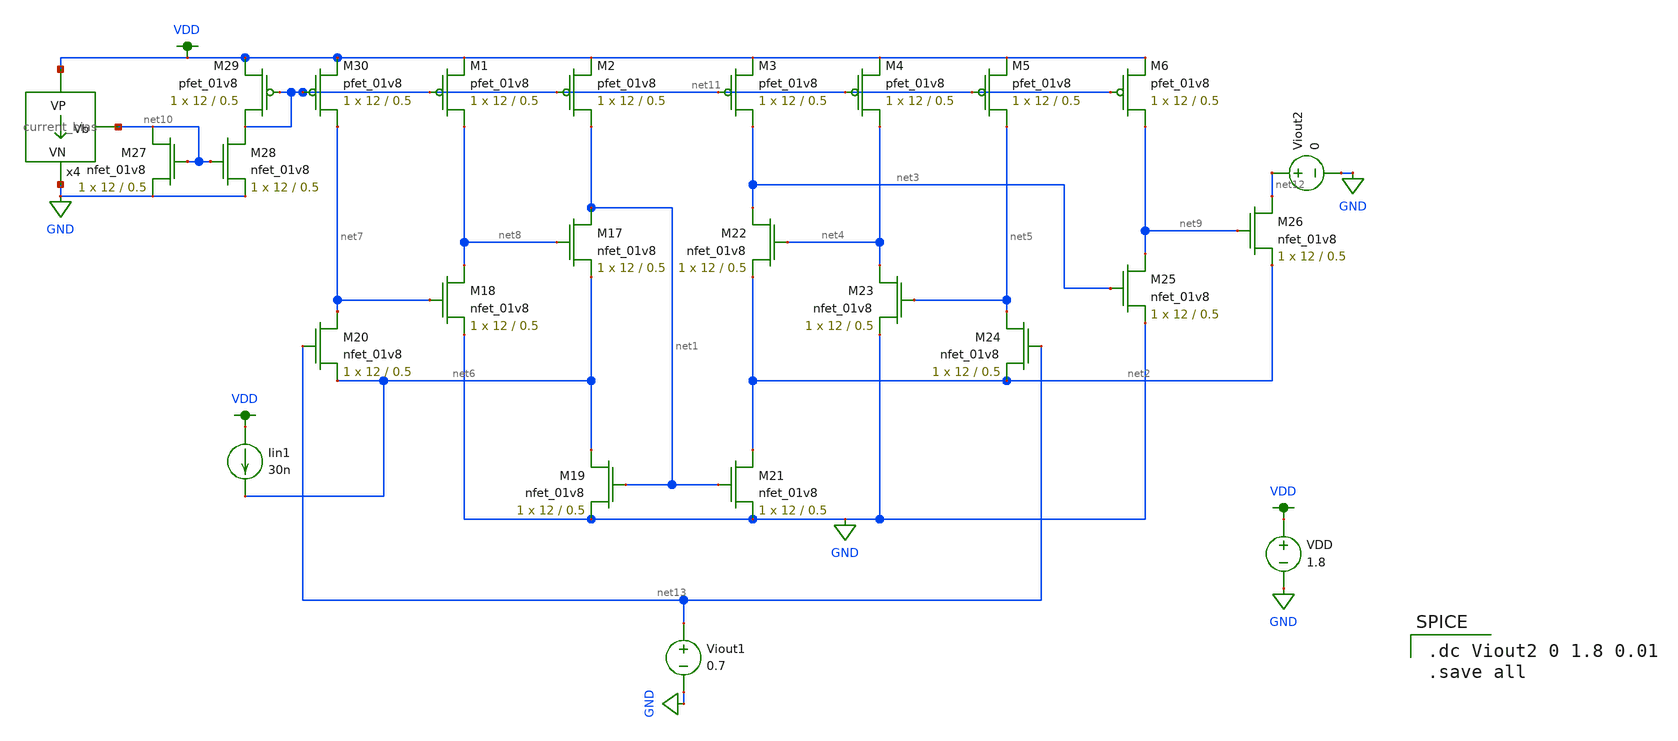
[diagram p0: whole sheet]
** sch_path: schematics/current mirrors/FVF_current_mirror_4_better.sch
**.subckt FVF_current_mirror_4_better
VDD VDD GND 1.8
XM19 net6 net1 GND GND sky130_fd_pr__nfet_01v8 L=0.5 W=12 nf=1 ad='int((nf+1)/2) * W/nf * 0.29' as='int((nf+2)/2) * W/nf * 0.29'
+ pd='2*int((nf+1)/2) * (W/nf + 0.29)' ps='2*int((nf+2)/2) * (W/nf + 0.29)' nrd='0.29 / W' nrs='0.29 / W'
+ sa=0 sb=0 sd=0 mult=1 m=1
XM21 net2 net1 GND GND sky130_fd_pr__nfet_01v8 L=0.5 W=12 nf=1 ad='int((nf+1)/2) * W/nf * 0.29' as='int((nf+2)/2) * W/nf * 0.29'
+ pd='2*int((nf+1)/2) * (W/nf + 0.29)' ps='2*int((nf+2)/2) * (W/nf + 0.29)' nrd='0.29 / W' nrs='0.29 / W'
+ sa=0 sb=0 sd=0 mult=1 m=1
XM22 net3 net4 net2 GND sky130_fd_pr__nfet_01v8 L=0.5 W=12 nf=1 ad='int((nf+1)/2) * W/nf * 0.29' as='int((nf+2)/2) * W/nf * 0.29'
+ pd='2*int((nf+1)/2) * (W/nf + 0.29)' ps='2*int((nf+2)/2) * (W/nf + 0.29)' nrd='0.29 / W' nrs='0.29 / W'
+ sa=0 sb=0 sd=0 mult=1 m=1
XM23 net4 net5 GND GND sky130_fd_pr__nfet_01v8 L=0.5 W=12 nf=1 ad='int((nf+1)/2) * W/nf * 0.29' as='int((nf+2)/2) * W/nf * 0.29'
+ pd='2*int((nf+1)/2) * (W/nf + 0.29)' ps='2*int((nf+2)/2) * (W/nf + 0.29)' nrd='0.29 / W' nrs='0.29 / W'
+ sa=0 sb=0 sd=0 mult=1 m=1
XM24 net5 net13 net2 GND sky130_fd_pr__nfet_01v8 L=0.5 W=12 nf=1 ad='int((nf+1)/2) * W/nf * 0.29' as='int((nf+2)/2) * W/nf * 0.29'
+ pd='2*int((nf+1)/2) * (W/nf + 0.29)' ps='2*int((nf+2)/2) * (W/nf + 0.29)' nrd='0.29 / W' nrs='0.29 / W'
+ sa=0 sb=0 sd=0 mult=1 m=1
XM17 net1 net8 net6 GND sky130_fd_pr__nfet_01v8 L=0.5 W=12 nf=1 ad='int((nf+1)/2) * W/nf * 0.29' as='int((nf+2)/2) * W/nf * 0.29'
+ pd='2*int((nf+1)/2) * (W/nf + 0.29)' ps='2*int((nf+2)/2) * (W/nf + 0.29)' nrd='0.29 / W' nrs='0.29 / W'
+ sa=0 sb=0 sd=0 mult=1 m=1
XM18 net8 net7 GND GND sky130_fd_pr__nfet_01v8 L=0.5 W=12 nf=1 ad='int((nf+1)/2) * W/nf * 0.29' as='int((nf+2)/2) * W/nf * 0.29'
+ pd='2*int((nf+1)/2) * (W/nf + 0.29)' ps='2*int((nf+2)/2) * (W/nf + 0.29)' nrd='0.29 / W' nrs='0.29 / W'
+ sa=0 sb=0 sd=0 mult=1 m=1
XM20 net7 net13 net6 GND sky130_fd_pr__nfet_01v8 L=0.5 W=12 nf=1 ad='int((nf+1)/2) * W/nf * 0.29' as='int((nf+2)/2) * W/nf * 0.29'
+ pd='2*int((nf+1)/2) * (W/nf + 0.29)' ps='2*int((nf+2)/2) * (W/nf + 0.29)' nrd='0.29 / W' nrs='0.29 / W'
+ sa=0 sb=0 sd=0 mult=1 m=1
XM25 net9 net3 GND GND sky130_fd_pr__nfet_01v8 L=0.5 W=12 nf=1 ad='int((nf+1)/2) * W/nf * 0.29' as='int((nf+2)/2) * W/nf * 0.29'
+ pd='2*int((nf+1)/2) * (W/nf + 0.29)' ps='2*int((nf+2)/2) * (W/nf + 0.29)' nrd='0.29 / W' nrs='0.29 / W'
+ sa=0 sb=0 sd=0 mult=1 m=1
XM26 net12 net9 net2 GND sky130_fd_pr__nfet_01v8 L=0.5 W=12 nf=1 ad='int((nf+1)/2) * W/nf * 0.29' as='int((nf+2)/2) * W/nf * 0.29'
+ pd='2*int((nf+1)/2) * (W/nf + 0.29)' ps='2*int((nf+2)/2) * (W/nf + 0.29)' nrd='0.29 / W' nrs='0.29 / W'
+ sa=0 sb=0 sd=0 mult=1 m=1
Iin1 VDD net6 30n
x4 VDD net10 GND current_bias
XM27 net10 net10 GND GND sky130_fd_pr__nfet_01v8 L=0.5 W=12 nf=1 ad='int((nf+1)/2) * W/nf * 0.29' as='int((nf+2)/2) * W/nf * 0.29'
+ pd='2*int((nf+1)/2) * (W/nf + 0.29)' ps='2*int((nf+2)/2) * (W/nf + 0.29)' nrd='0.29 / W' nrs='0.29 / W'
+ sa=0 sb=0 sd=0 mult=1 m=1
XM28 net11 net10 GND GND sky130_fd_pr__nfet_01v8 L=0.5 W=12 nf=1 ad='int((nf+1)/2) * W/nf * 0.29' as='int((nf+2)/2) * W/nf * 0.29'
+ pd='2*int((nf+1)/2) * (W/nf + 0.29)' ps='2*int((nf+2)/2) * (W/nf + 0.29)' nrd='0.29 / W' nrs='0.29 / W'
+ sa=0 sb=0 sd=0 mult=1 m=1
XM29 net11 net11 VDD VDD sky130_fd_pr__pfet_01v8 L=0.5 W=12 nf=1 ad='int((nf+1)/2) * W/nf * 0.29' as='int((nf+2)/2) * W/nf * 0.29'
+ pd='2*int((nf+1)/2) * (W/nf + 0.29)' ps='2*int((nf+2)/2) * (W/nf + 0.29)' nrd='0.29 / W' nrs='0.29 / W'
+ sa=0 sb=0 sd=0 mult=1 m=1
XM30 net7 net11 VDD VDD sky130_fd_pr__pfet_01v8 L=0.5 W=12 nf=1 ad='int((nf+1)/2) * W/nf * 0.29' as='int((nf+2)/2) * W/nf * 0.29'
+ pd='2*int((nf+1)/2) * (W/nf + 0.29)' ps='2*int((nf+2)/2) * (W/nf + 0.29)' nrd='0.29 / W' nrs='0.29 / W'
+ sa=0 sb=0 sd=0 mult=1 m=1
Viout2 net12 GND 0
Viout1 net13 GND 0.7
XM1 net8 net11 VDD VDD sky130_fd_pr__pfet_01v8 L=0.5 W=12 nf=1 ad='int((nf+1)/2) * W/nf * 0.29' as='int((nf+2)/2) * W/nf * 0.29'
+ pd='2*int((nf+1)/2) * (W/nf + 0.29)' ps='2*int((nf+2)/2) * (W/nf + 0.29)' nrd='0.29 / W' nrs='0.29 / W'
+ sa=0 sb=0 sd=0 mult=1 m=1
XM2 net1 net11 VDD VDD sky130_fd_pr__pfet_01v8 L=0.5 W=12 nf=1 ad='int((nf+1)/2) * W/nf * 0.29' as='int((nf+2)/2) * W/nf * 0.29'
+ pd='2*int((nf+1)/2) * (W/nf + 0.29)' ps='2*int((nf+2)/2) * (W/nf + 0.29)' nrd='0.29 / W' nrs='0.29 / W'
+ sa=0 sb=0 sd=0 mult=1 m=1
XM3 net3 net11 VDD VDD sky130_fd_pr__pfet_01v8 L=0.5 W=12 nf=1 ad='int((nf+1)/2) * W/nf * 0.29' as='int((nf+2)/2) * W/nf * 0.29'
+ pd='2*int((nf+1)/2) * (W/nf + 0.29)' ps='2*int((nf+2)/2) * (W/nf + 0.29)' nrd='0.29 / W' nrs='0.29 / W'
+ sa=0 sb=0 sd=0 mult=1 m=1
XM4 net4 net11 VDD VDD sky130_fd_pr__pfet_01v8 L=0.5 W=12 nf=1 ad='int((nf+1)/2) * W/nf * 0.29' as='int((nf+2)/2) * W/nf * 0.29'
+ pd='2*int((nf+1)/2) * (W/nf + 0.29)' ps='2*int((nf+2)/2) * (W/nf + 0.29)' nrd='0.29 / W' nrs='0.29 / W'
+ sa=0 sb=0 sd=0 mult=1 m=1
XM5 net5 net11 VDD VDD sky130_fd_pr__pfet_01v8 L=0.5 W=12 nf=1 ad='int((nf+1)/2) * W/nf * 0.29' as='int((nf+2)/2) * W/nf * 0.29'
+ pd='2*int((nf+1)/2) * (W/nf + 0.29)' ps='2*int((nf+2)/2) * (W/nf + 0.29)' nrd='0.29 / W' nrs='0.29 / W'
+ sa=0 sb=0 sd=0 mult=1 m=1
XM6 net9 net11 VDD VDD sky130_fd_pr__pfet_01v8 L=0.5 W=12 nf=1 ad='int((nf+1)/2) * W/nf * 0.29' as='int((nf+2)/2) * W/nf * 0.29'
+ pd='2*int((nf+1)/2) * (W/nf + 0.29)' ps='2*int((nf+2)/2) * (W/nf + 0.29)' nrd='0.29 / W' nrs='0.29 / W'
+ sa=0 sb=0 sd=0 mult=1 m=1
**** begin user architecture code

.option wnflag=1
.param MC_SWITCH=0.0
.lib ~/skywater/skywater-pdk/libraries/sky130_fd_pr_ngspice/latest/models/sky130.lib.spice tt


.dc Viout2 0 1.8 0.01
.save all

**** end user architecture code
**.ends
.GLOBAL VDD
.GLOBAL GND
.end
